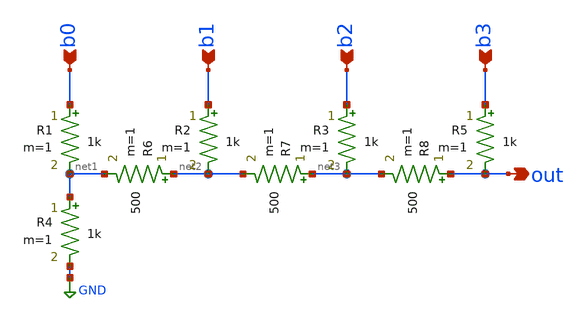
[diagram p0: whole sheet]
** sch_path: xschem/r2r.sch
**.subckt r2r b1 out b0 b2 b3
*.ipin b1
*.opin out
*.ipin b0
*.ipin b2
*.ipin b3
R1 b0 net1 1k m=1
R2 b1 net2 1k m=1
R3 b2 net3 1k m=1
R4 net1 GND 1k m=1
R5 b3 out 1k m=1
R6 net2 net1 500 m=1
R7 net3 net2 500 m=1
R8 out net3 500 m=1
**.ends
.GLOBAL GND
.end
